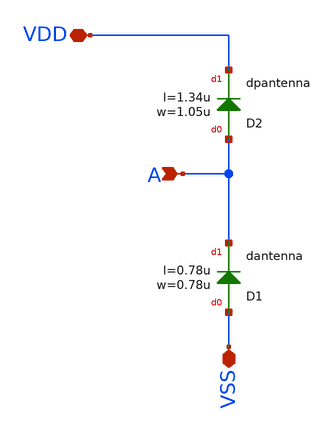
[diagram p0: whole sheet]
** sch_path: ihp-sg13g2/libs.tech/xschem/sg13g2_stdcells/sg13g2_antennanp.sch
* Copyright 2023 IHP PDK Authors
* Licensed under the Apache License, Version 2.0 (the "License");
* you may not use this file except in compliance with the License.
* You may obtain a copy of the License at
* https://www.apache.org/licenses/LICENSE-2.0
* Unless required by applicable law or agreed to in writing, software
* distributed under the License is distributed on an "AS IS" BASIS,
* WITHOUT WARRANTIES OR CONDITIONS OF ANY KIND, either express or implied.
* See the License for the specific language governing permissions and
* limitations under the License.
**.subckt sg13g2_antennanp A VDD VSS
*.ipin A
*.iopin VDD
*.iopin VSS
XD1 VSS A dantenna l=0.78u w=0.78u
XD2 A VDD dpantenna l=1.34u w=1.05u
**.ends
.end
